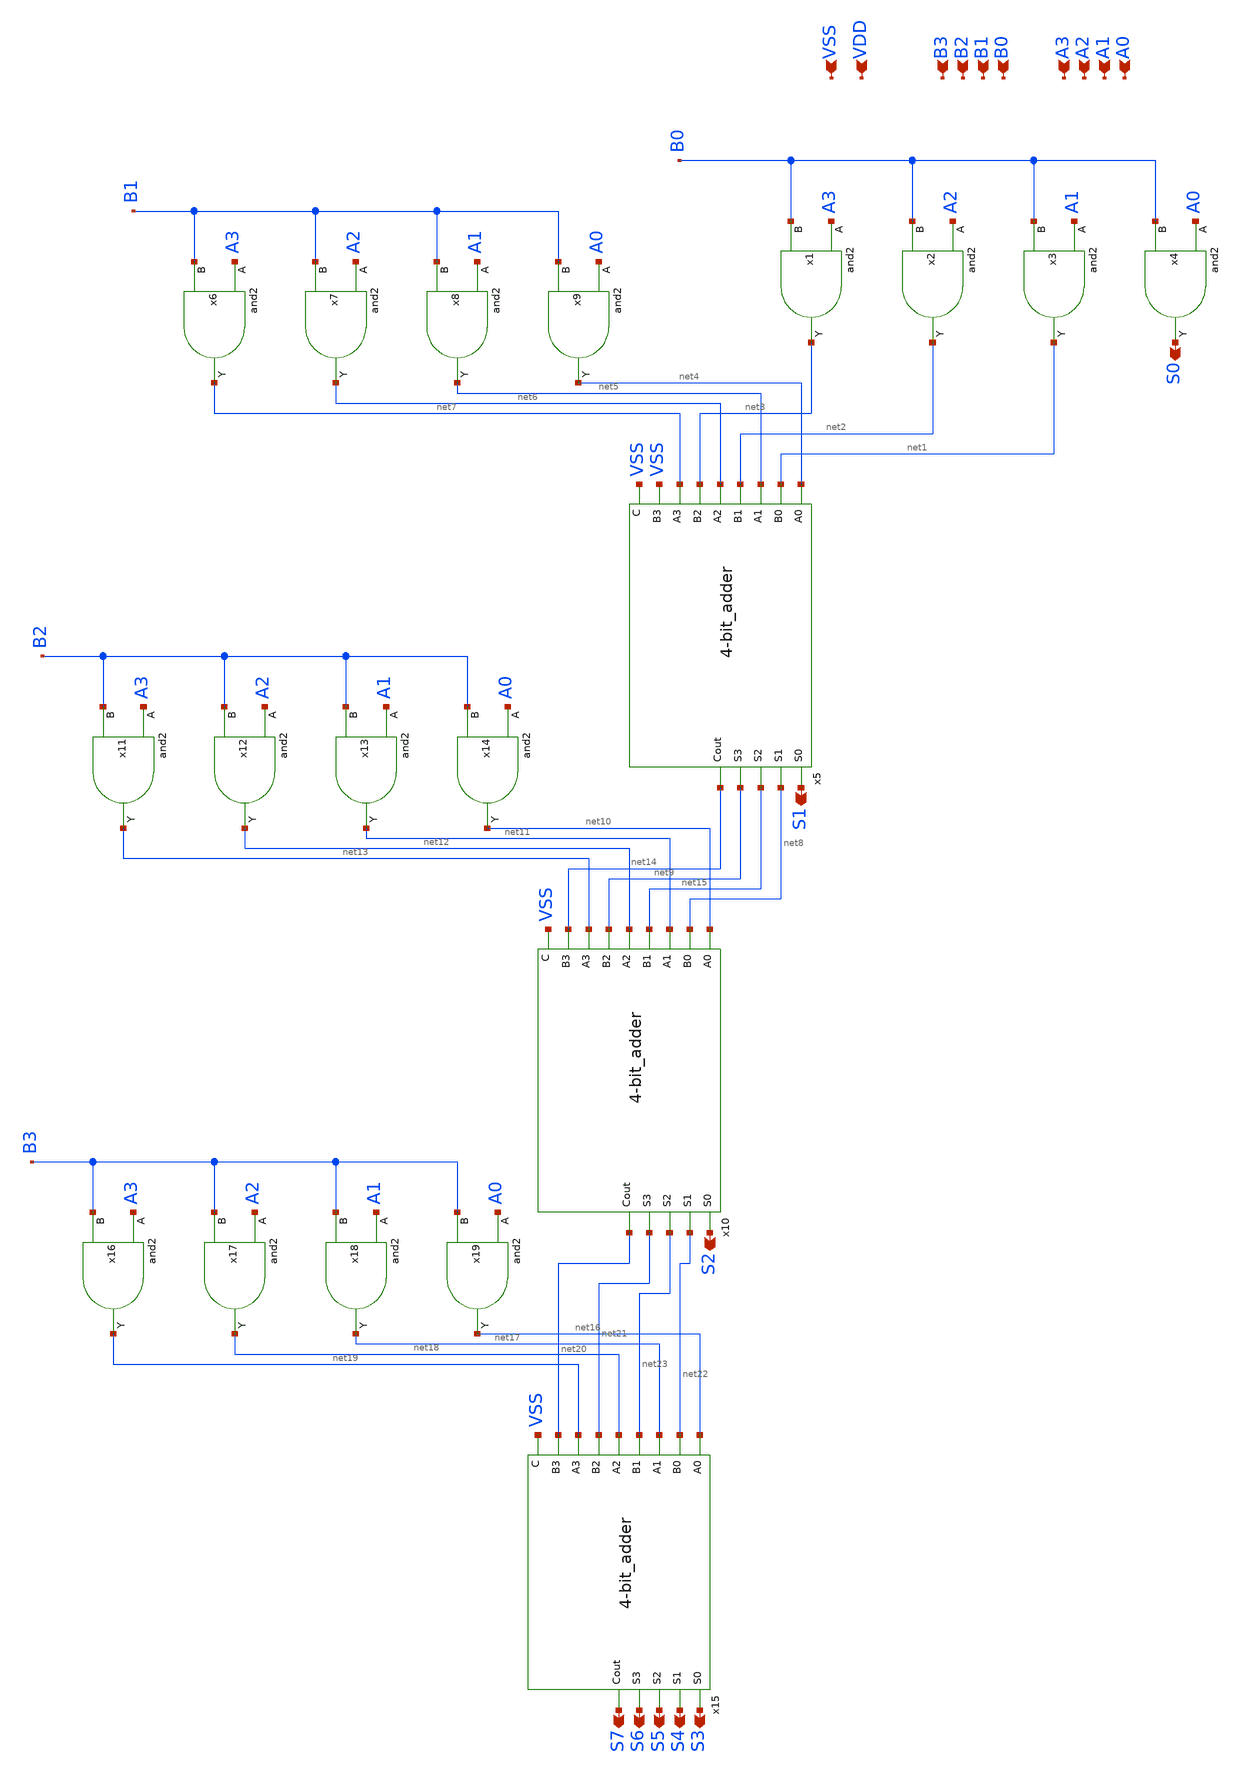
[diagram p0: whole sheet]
** sch_path: design/xschem/MULTIPLIER/mul.sch
**.subckt mul A0 A1 A2 A3 B1 B2 B3 B0 S6 S7 S3 S4 S5 S0 S1 S2 VSS VDD
*.ipin A0
*.ipin A1
*.ipin A2
*.ipin A3
*.ipin B1
*.ipin B2
*.ipin B3
*.ipin B0
*.opin S6
*.opin S7
*.opin S3
*.opin S4
*.opin S5
*.opin S0
*.opin S1
*.opin S2
*.ipin VSS
*.ipin VDD
x1 A3 B0 VSS VDD net3 and2
x2 A2 B0 VSS VDD net2 and2
x3 A1 B0 VSS VDD net1 and2
x4 A0 B0 VSS VDD S0 and2
x5 net4 S1 net1 net5 net8 net2 net6 net15 net3 net7 net9 VSS net14 VSS VSS VDD 4-bit_adder
x6 A3 B1 VSS VDD net7 and2
x7 A2 B1 VSS VDD net6 and2
x8 A1 B1 VSS VDD net5 and2
x9 A0 B1 VSS VDD net4 and2
x10 net10 S2 net8 net11 net22 net15 net12 net23 net9 net13 net21 net14 net20 VSS VSS VDD 4-bit_adder
x11 A3 B2 VSS VDD net13 and2
x12 A2 B2 VSS VDD net12 and2
x13 A1 B2 VSS VDD net11 and2
x14 A0 B2 VSS VDD net10 and2
x15 net16 S3 net22 net17 S4 net23 net18 S5 net21 net19 S6 net20 S7 VSS VSS VDD 4-bit_adder
x16 A3 B3 VSS VDD net19 and2
x17 A2 B3 VSS VDD net18 and2
x18 A1 B3 VSS VDD net17 and2
x19 A0 B3 VSS VDD net16 and2
**.ends
.end
